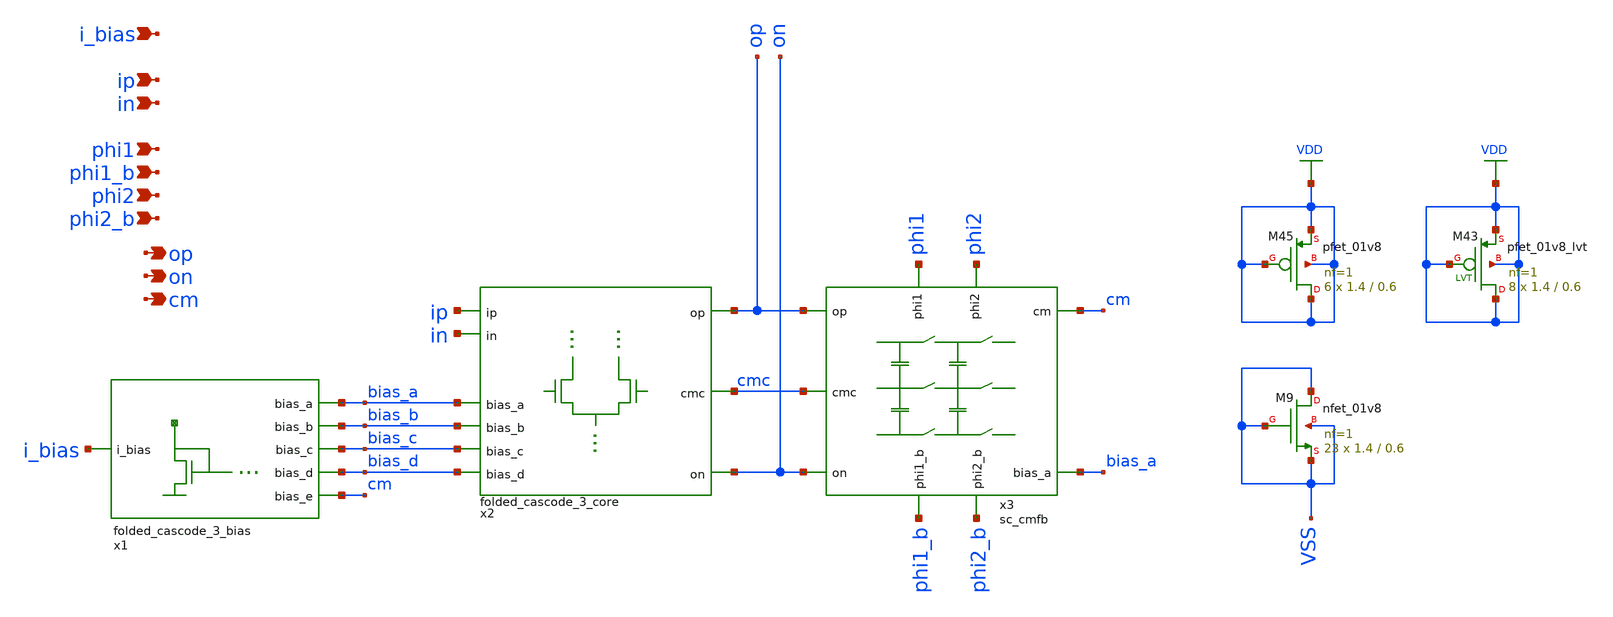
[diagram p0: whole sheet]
** sch_path: design/analog_modulator/schematic/ota.sch
**.subckt ota ip in phi1 phi1_b phi2 phi2_b op on i_bias cm
*.ipin ip
*.ipin in
*.ipin phi1
*.ipin phi1_b
*.ipin phi2
*.ipin phi2_b
*.opin op
*.opin on
*.ipin i_bias
*.opin cm
x1 bias_a bias_b bias_c bias_d cm i_bias VDD VSS folded_cascode_3_bias
x3 phi1 phi1_b op on cm bias_a cmc phi2 phi2_b VDD VSS sc_cmfb
x2 cmc ip in bias_a bias_b bias_c bias_d op on VDD VSS folded_cascode_3_core
XM43 VDD VDD VDD VDD sky130_fd_pr__pfet_01v8_lvt L=0.6 W=1.4 nf=1 ad='int((nf+1)/2) * W/nf * 0.29' as='int((nf+2)/2) * W/nf * 0.29'
+ pd='2*int((nf+1)/2) * (W/nf + 0.29)' ps='2*int((nf+2)/2) * (W/nf + 0.29)' nrd='0.29 / W' nrs='0.29 / W'
+ sa=0 sb=0 sd=0 mult=8 m=8
XM45 VDD VDD VDD VDD sky130_fd_pr__pfet_01v8 L=0.6 W=1.4 nf=1 ad='int((nf+1)/2) * W/nf * 0.29' as='int((nf+2)/2) * W/nf * 0.29'
+ pd='2*int((nf+1)/2) * (W/nf + 0.29)' ps='2*int((nf+2)/2) * (W/nf + 0.29)' nrd='0.29 / W' nrs='0.29 / W'
+ sa=0 sb=0 sd=0 mult=6 m=6
XM9 VSS VSS VSS VSS sky130_fd_pr__nfet_01v8 L=0.6 W=1.4 nf=1 ad='int((nf+1)/2) * W/nf * 0.29' as='int((nf+2)/2) * W/nf * 0.29'
+ pd='2*int((nf+1)/2) * (W/nf + 0.29)' ps='2*int((nf+2)/2) * (W/nf + 0.29)' nrd='0.29 / W' nrs='0.29 / W'
+ sa=0 sb=0 sd=0 mult=23 m=23
**.ends

* expanding   symbol:  folded_cascode_3_bias.sym # of pins=6
** sym_path: design/analog_modulator/schematic/folded_cascode_3_bias.sym
** sch_path: design/analog_modulator/schematic/folded_cascode_3_bias.sch
.subckt folded_cascode_3_bias bias_a bias_b bias_c bias_d bias_e i_bias VDD VSS
*.opin bias_a
*.opin bias_b
*.opin bias_c
*.opin bias_d
*.opin bias_e
*.ipin i_bias
XM22 bias_b bias_c m21d VDD sky130_fd_pr__pfet_01v8 L=0.6 W=1.4 nf=1 ad='int((nf+1)/2) * W/nf * 0.29'
+ as='int((nf+2)/2) * W/nf * 0.29' pd='2*int((nf+1)/2) * (W/nf + 0.29)' ps='2*int((nf+2)/2) * (W/nf + 0.29)'
+ nrd='0.29 / W' nrs='0.29 / W' sa=0 sb=0 sd=0 mult=6 m=6
XM26 m2d bias_c m25d VDD sky130_fd_pr__pfet_01v8 L=0.6 W=1.4 nf=1 ad='int((nf+1)/2) * W/nf * 0.29' as='int((nf+2)/2) * W/nf * 0.29'
+ pd='2*int((nf+1)/2) * (W/nf + 0.29)' ps='2*int((nf+2)/2) * (W/nf + 0.29)' nrd='0.29 / W' nrs='0.29 / W'
+ sa=0 sb=0 sd=0 mult=6 m=6
XM32 bias_e bias_c m31d VDD sky130_fd_pr__pfet_01v8 L=0.6 W=1.4 nf=1 ad='int((nf+1)/2) * W/nf * 0.29'
+ as='int((nf+2)/2) * W/nf * 0.29' pd='2*int((nf+1)/2) * (W/nf + 0.29)' ps='2*int((nf+2)/2) * (W/nf + 0.29)'
+ nrd='0.29 / W' nrs='0.29 / W' sa=0 sb=0 sd=0 mult=6 m=6
XM21 m21d bias_b VDD VDD sky130_fd_pr__pfet_01v8_lvt L=0.6 W=1.4 nf=1 ad='int((nf+1)/2) * W/nf * 0.29'
+ as='int((nf+2)/2) * W/nf * 0.29' pd='2*int((nf+1)/2) * (W/nf + 0.29)' ps='2*int((nf+2)/2) * (W/nf + 0.29)'
+ nrd='0.29 / W' nrs='0.29 / W' sa=0 sb=0 sd=0 mult=6 m=6
XM25 m25d bias_b VDD VDD sky130_fd_pr__pfet_01v8_lvt L=0.6 W=1.4 nf=1 ad='int((nf+1)/2) * W/nf * 0.29'
+ as='int((nf+2)/2) * W/nf * 0.29' pd='2*int((nf+1)/2) * (W/nf + 0.29)' ps='2*int((nf+2)/2) * (W/nf + 0.29)'
+ nrd='0.29 / W' nrs='0.29 / W' sa=0 sb=0 sd=0 mult=6 m=6
XM31 m31d bias_b VDD VDD sky130_fd_pr__pfet_01v8_lvt L=0.6 W=1.4 nf=1 ad='int((nf+1)/2) * W/nf * 0.29'
+ as='int((nf+2)/2) * W/nf * 0.29' pd='2*int((nf+1)/2) * (W/nf + 0.29)' ps='2*int((nf+2)/2) * (W/nf + 0.29)'
+ nrd='0.29 / W' nrs='0.29 / W' sa=0 sb=0 sd=0 mult=6 m=6
XM1 bias_b bias_b bias_c VSS sky130_fd_pr__nfet_01v8_lvt L=0.6 W=1.4 nf=1 ad='int((nf+1)/2) * W/nf * 0.29'
+ as='int((nf+2)/2) * W/nf * 0.29' pd='2*int((nf+1)/2) * (W/nf + 0.29)' ps='2*int((nf+2)/2) * (W/nf + 0.29)'
+ nrd='0.29 / W' nrs='0.29 / W' sa=0 sb=0 sd=0 mult=56 m=56
XM2 m2d m2d bias_d VSS sky130_fd_pr__nfet_01v8 L=0.6 W=1.4 nf=1 ad='int((nf+1)/2) * W/nf * 0.29' as='int((nf+2)/2) * W/nf * 0.29'
+ pd='2*int((nf+1)/2) * (W/nf + 0.29)' ps='2*int((nf+2)/2) * (W/nf + 0.29)' nrd='0.29 / W' nrs='0.29 / W'
+ sa=0 sb=0 sd=0 mult=50 m=50
XM3 bias_d m2d bias_a VSS sky130_fd_pr__nfet_01v8 L=0.6 W=1.4 nf=1 ad='int((nf+1)/2) * W/nf * 0.29' as='int((nf+2)/2) * W/nf * 0.29'
+ pd='2*int((nf+1)/2) * (W/nf + 0.29)' ps='2*int((nf+2)/2) * (W/nf + 0.29)' nrd='0.29 / W' nrs='0.29 / W'
+ sa=0 sb=0 sd=0 mult=2 m=2
XM4 bias_a bias_d m5d VSS sky130_fd_pr__nfet_01v8 L=0.6 W=1.4 nf=1 ad='int((nf+1)/2) * W/nf * 0.29' as='int((nf+2)/2) * W/nf * 0.29'
+ pd='2*int((nf+1)/2) * (W/nf + 0.29)' ps='2*int((nf+2)/2) * (W/nf + 0.29)' nrd='0.29 / W' nrs='0.29 / W'
+ sa=0 sb=0 sd=0 mult=18 m=18
XM5 m5d bias_a VSS VSS sky130_fd_pr__nfet_01v8 L=0.6 W=1.4 nf=1 ad='int((nf+1)/2) * W/nf * 0.29' as='int((nf+2)/2) * W/nf * 0.29'
+ pd='2*int((nf+1)/2) * (W/nf + 0.29)' ps='2*int((nf+2)/2) * (W/nf + 0.29)' nrd='0.29 / W' nrs='0.29 / W'
+ sa=0 sb=0 sd=0 mult=18 m=18
XM6 bias_c i_bias VSS VSS sky130_fd_pr__nfet_01v8 L=0.6 W=1.4 nf=1 ad='int((nf+1)/2) * W/nf * 0.29' as='int((nf+2)/2) * W/nf * 0.29'
+ pd='2*int((nf+1)/2) * (W/nf + 0.29)' ps='2*int((nf+2)/2) * (W/nf + 0.29)' nrd='0.29 / W' nrs='0.29 / W'
+ sa=0 sb=0 sd=0 mult=18 m=18
XM7 i_bias i_bias VSS VSS sky130_fd_pr__nfet_01v8 L=0.6 W=1.4 nf=1 ad='int((nf+1)/2) * W/nf * 0.29' as='int((nf+2)/2) * W/nf * 0.29'
+ pd='2*int((nf+1)/2) * (W/nf + 0.29)' ps='2*int((nf+2)/2) * (W/nf + 0.29)' nrd='0.29 / W' nrs='0.29 / W'
+ sa=0 sb=0 sd=0 mult=18 m=18
XM33 bias_e bias_e net1 VSS sky130_fd_pr__nfet_01v8 L=0.6 W=1.4 nf=1 ad='int((nf+1)/2) * W/nf * 0.29'
+ as='int((nf+2)/2) * W/nf * 0.29' pd='2*int((nf+1)/2) * (W/nf + 0.29)' ps='2*int((nf+2)/2) * (W/nf + 0.29)'
+ nrd='0.29 / W' nrs='0.29 / W' sa=0 sb=0 sd=0 mult=1 m=1
XM49 net1 bias_e net2 VSS sky130_fd_pr__nfet_01v8 L=0.6 W=1.4 nf=1 ad='int((nf+1)/2) * W/nf * 0.29' as='int((nf+2)/2) * W/nf * 0.29'
+ pd='2*int((nf+1)/2) * (W/nf + 0.29)' ps='2*int((nf+2)/2) * (W/nf + 0.29)' nrd='0.29 / W' nrs='0.29 / W'
+ sa=0 sb=0 sd=0 mult=1 m=1
XM50 net2 bias_e net3 VSS sky130_fd_pr__nfet_01v8 L=0.6 W=1.4 nf=1 ad='int((nf+1)/2) * W/nf * 0.29' as='int((nf+2)/2) * W/nf * 0.29'
+ pd='2*int((nf+1)/2) * (W/nf + 0.29)' ps='2*int((nf+2)/2) * (W/nf + 0.29)' nrd='0.29 / W' nrs='0.29 / W'
+ sa=0 sb=0 sd=0 mult=1 m=1
XM63 net3 bias_e VSS VSS sky130_fd_pr__nfet_01v8 L=0.6 W=1.4 nf=1 ad='int((nf+1)/2) * W/nf * 0.29' as='int((nf+2)/2) * W/nf * 0.29'
+ pd='2*int((nf+1)/2) * (W/nf + 0.29)' ps='2*int((nf+2)/2) * (W/nf + 0.29)' nrd='0.29 / W' nrs='0.29 / W'
+ sa=0 sb=0 sd=0 mult=1 m=1
XM68 bias_e bias_e net4 VSS sky130_fd_pr__nfet_01v8 L=0.6 W=1.4 nf=1 ad='int((nf+1)/2) * W/nf * 0.29'
+ as='int((nf+2)/2) * W/nf * 0.29' pd='2*int((nf+1)/2) * (W/nf + 0.29)' ps='2*int((nf+2)/2) * (W/nf + 0.29)'
+ nrd='0.29 / W' nrs='0.29 / W' sa=0 sb=0 sd=0 mult=1 m=1
XM69 net4 bias_e net5 VSS sky130_fd_pr__nfet_01v8 L=0.6 W=1.4 nf=1 ad='int((nf+1)/2) * W/nf * 0.29' as='int((nf+2)/2) * W/nf * 0.29'
+ pd='2*int((nf+1)/2) * (W/nf + 0.29)' ps='2*int((nf+2)/2) * (W/nf + 0.29)' nrd='0.29 / W' nrs='0.29 / W'
+ sa=0 sb=0 sd=0 mult=1 m=1
XM70 net5 bias_e net6 VSS sky130_fd_pr__nfet_01v8 L=0.6 W=1.4 nf=1 ad='int((nf+1)/2) * W/nf * 0.29' as='int((nf+2)/2) * W/nf * 0.29'
+ pd='2*int((nf+1)/2) * (W/nf + 0.29)' ps='2*int((nf+2)/2) * (W/nf + 0.29)' nrd='0.29 / W' nrs='0.29 / W'
+ sa=0 sb=0 sd=0 mult=1 m=1
XM71 net6 bias_e VSS VSS sky130_fd_pr__nfet_01v8 L=0.6 W=1.4 nf=1 ad='int((nf+1)/2) * W/nf * 0.29' as='int((nf+2)/2) * W/nf * 0.29'
+ pd='2*int((nf+1)/2) * (W/nf + 0.29)' ps='2*int((nf+2)/2) * (W/nf + 0.29)' nrd='0.29 / W' nrs='0.29 / W'
+ sa=0 sb=0 sd=0 mult=1 m=1
XM72 bias_e bias_e net7 VSS sky130_fd_pr__nfet_01v8 L=0.6 W=1.4 nf=1 ad='int((nf+1)/2) * W/nf * 0.29'
+ as='int((nf+2)/2) * W/nf * 0.29' pd='2*int((nf+1)/2) * (W/nf + 0.29)' ps='2*int((nf+2)/2) * (W/nf + 0.29)'
+ nrd='0.29 / W' nrs='0.29 / W' sa=0 sb=0 sd=0 mult=1 m=1
XM73 net7 bias_e net8 VSS sky130_fd_pr__nfet_01v8 L=0.6 W=1.4 nf=1 ad='int((nf+1)/2) * W/nf * 0.29' as='int((nf+2)/2) * W/nf * 0.29'
+ pd='2*int((nf+1)/2) * (W/nf + 0.29)' ps='2*int((nf+2)/2) * (W/nf + 0.29)' nrd='0.29 / W' nrs='0.29 / W'
+ sa=0 sb=0 sd=0 mult=1 m=1
XM74 net8 bias_e net9 VSS sky130_fd_pr__nfet_01v8 L=0.6 W=1.4 nf=1 ad='int((nf+1)/2) * W/nf * 0.29' as='int((nf+2)/2) * W/nf * 0.29'
+ pd='2*int((nf+1)/2) * (W/nf + 0.29)' ps='2*int((nf+2)/2) * (W/nf + 0.29)' nrd='0.29 / W' nrs='0.29 / W'
+ sa=0 sb=0 sd=0 mult=1 m=1
XM75 net9 bias_e VSS VSS sky130_fd_pr__nfet_01v8 L=0.6 W=1.4 nf=1 ad='int((nf+1)/2) * W/nf * 0.29' as='int((nf+2)/2) * W/nf * 0.29'
+ pd='2*int((nf+1)/2) * (W/nf + 0.29)' ps='2*int((nf+2)/2) * (W/nf + 0.29)' nrd='0.29 / W' nrs='0.29 / W'
+ sa=0 sb=0 sd=0 mult=1 m=1
XM76 bias_e bias_e net10 VSS sky130_fd_pr__nfet_01v8 L=0.6 W=1.4 nf=1 ad='int((nf+1)/2) * W/nf * 0.29'
+ as='int((nf+2)/2) * W/nf * 0.29' pd='2*int((nf+1)/2) * (W/nf + 0.29)' ps='2*int((nf+2)/2) * (W/nf + 0.29)'
+ nrd='0.29 / W' nrs='0.29 / W' sa=0 sb=0 sd=0 mult=1 m=1
XM77 net10 bias_e net11 VSS sky130_fd_pr__nfet_01v8 L=0.6 W=1.4 nf=1 ad='int((nf+1)/2) * W/nf * 0.29'
+ as='int((nf+2)/2) * W/nf * 0.29' pd='2*int((nf+1)/2) * (W/nf + 0.29)' ps='2*int((nf+2)/2) * (W/nf + 0.29)'
+ nrd='0.29 / W' nrs='0.29 / W' sa=0 sb=0 sd=0 mult=1 m=1
XM78 net11 bias_e net12 VSS sky130_fd_pr__nfet_01v8 L=0.6 W=1.4 nf=1 ad='int((nf+1)/2) * W/nf * 0.29'
+ as='int((nf+2)/2) * W/nf * 0.29' pd='2*int((nf+1)/2) * (W/nf + 0.29)' ps='2*int((nf+2)/2) * (W/nf + 0.29)'
+ nrd='0.29 / W' nrs='0.29 / W' sa=0 sb=0 sd=0 mult=1 m=1
XM79 net12 bias_e VSS VSS sky130_fd_pr__nfet_01v8 L=0.6 W=1.4 nf=1 ad='int((nf+1)/2) * W/nf * 0.29' as='int((nf+2)/2) * W/nf * 0.29'
+ pd='2*int((nf+1)/2) * (W/nf + 0.29)' ps='2*int((nf+2)/2) * (W/nf + 0.29)' nrd='0.29 / W' nrs='0.29 / W'
+ sa=0 sb=0 sd=0 mult=1 m=1
XM64 bias_e bias_e net13 VSS sky130_fd_pr__nfet_01v8 L=0.6 W=1.4 nf=1 ad='int((nf+1)/2) * W/nf * 0.29'
+ as='int((nf+2)/2) * W/nf * 0.29' pd='2*int((nf+1)/2) * (W/nf + 0.29)' ps='2*int((nf+2)/2) * (W/nf + 0.29)'
+ nrd='0.29 / W' nrs='0.29 / W' sa=0 sb=0 sd=0 mult=1 m=1
XM65 net13 bias_e net14 VSS sky130_fd_pr__nfet_01v8 L=0.6 W=1.4 nf=1 ad='int((nf+1)/2) * W/nf * 0.29'
+ as='int((nf+2)/2) * W/nf * 0.29' pd='2*int((nf+1)/2) * (W/nf + 0.29)' ps='2*int((nf+2)/2) * (W/nf + 0.29)'
+ nrd='0.29 / W' nrs='0.29 / W' sa=0 sb=0 sd=0 mult=1 m=1
XM66 net14 bias_e net15 VSS sky130_fd_pr__nfet_01v8 L=0.6 W=1.4 nf=1 ad='int((nf+1)/2) * W/nf * 0.29'
+ as='int((nf+2)/2) * W/nf * 0.29' pd='2*int((nf+1)/2) * (W/nf + 0.29)' ps='2*int((nf+2)/2) * (W/nf + 0.29)'
+ nrd='0.29 / W' nrs='0.29 / W' sa=0 sb=0 sd=0 mult=1 m=1
XM67 net15 bias_e VSS VSS sky130_fd_pr__nfet_01v8 L=0.6 W=1.4 nf=1 ad='int((nf+1)/2) * W/nf * 0.29' as='int((nf+2)/2) * W/nf * 0.29'
+ pd='2*int((nf+1)/2) * (W/nf + 0.29)' ps='2*int((nf+2)/2) * (W/nf + 0.29)' nrd='0.29 / W' nrs='0.29 / W'
+ sa=0 sb=0 sd=0 mult=1 m=1
XM57 bias_b VDD VDD VDD sky130_fd_pr__pfet_01v8 L=0.6 W=1.4 nf=1 ad='int((nf+1)/2) * W/nf * 0.29' as='int((nf+2)/2) * W/nf * 0.29'
+ pd='2*int((nf+1)/2) * (W/nf + 0.29)' ps='2*int((nf+2)/2) * (W/nf + 0.29)' nrd='0.29 / W' nrs='0.29 / W'
+ sa=0 sb=0 sd=0 mult=2 m=2
XM58 m2d VDD VDD VDD sky130_fd_pr__pfet_01v8 L=0.6 W=1.4 nf=1 ad='int((nf+1)/2) * W/nf * 0.29' as='int((nf+2)/2) * W/nf * 0.29'
+ pd='2*int((nf+1)/2) * (W/nf + 0.29)' ps='2*int((nf+2)/2) * (W/nf + 0.29)' nrd='0.29 / W' nrs='0.29 / W'
+ sa=0 sb=0 sd=0 mult=2 m=2
XM59 bias_e VDD VDD VDD sky130_fd_pr__pfet_01v8 L=0.6 W=1.4 nf=1 ad='int((nf+1)/2) * W/nf * 0.29' as='int((nf+2)/2) * W/nf * 0.29'
+ pd='2*int((nf+1)/2) * (W/nf + 0.29)' ps='2*int((nf+2)/2) * (W/nf + 0.29)' nrd='0.29 / W' nrs='0.29 / W'
+ sa=0 sb=0 sd=0 mult=2 m=2
XM60 m31d VDD VDD VDD sky130_fd_pr__pfet_01v8 L=0.6 W=1.4 nf=1 ad='int((nf+1)/2) * W/nf * 0.29' as='int((nf+2)/2) * W/nf * 0.29'
+ pd='2*int((nf+1)/2) * (W/nf + 0.29)' ps='2*int((nf+2)/2) * (W/nf + 0.29)' nrd='0.29 / W' nrs='0.29 / W'
+ sa=0 sb=0 sd=0 mult=2 m=2
XM42 m5d VSS VSS VSS sky130_fd_pr__nfet_01v8 L=0.6 W=1.4 nf=1 ad='int((nf+1)/2) * W/nf * 0.29' as='int((nf+2)/2) * W/nf * 0.29'
+ pd='2*int((nf+1)/2) * (W/nf + 0.29)' ps='2*int((nf+2)/2) * (W/nf + 0.29)' nrd='0.29 / W' nrs='0.29 / W'
+ sa=0 sb=0 sd=0 mult=6 m=6
XM44 bias_c bias_c bias_c VSS sky130_fd_pr__nfet_01v8 L=0.6 W=1.4 nf=1 ad='int((nf+1)/2) * W/nf * 0.29'
+ as='int((nf+2)/2) * W/nf * 0.29' pd='2*int((nf+1)/2) * (W/nf + 0.29)' ps='2*int((nf+2)/2) * (W/nf + 0.29)'
+ nrd='0.29 / W' nrs='0.29 / W' sa=0 sb=0 sd=0 mult=2 m=2
XM34 bias_d bias_d bias_d VSS sky130_fd_pr__nfet_01v8 L=0.6 W=1.4 nf=1 ad='int((nf+1)/2) * W/nf * 0.29'
+ as='int((nf+2)/2) * W/nf * 0.29' pd='2*int((nf+1)/2) * (W/nf + 0.29)' ps='2*int((nf+2)/2) * (W/nf + 0.29)'
+ nrd='0.29 / W' nrs='0.29 / W' sa=0 sb=0 sd=0 mult=8 m=8
XM35 m2d m2d m2d VSS sky130_fd_pr__nfet_01v8 L=0.6 W=1.4 nf=1 ad='int((nf+1)/2) * W/nf * 0.29' as='int((nf+2)/2) * W/nf * 0.29'
+ pd='2*int((nf+1)/2) * (W/nf + 0.29)' ps='2*int((nf+2)/2) * (W/nf + 0.29)' nrd='0.29 / W' nrs='0.29 / W'
+ sa=0 sb=0 sd=0 mult=2 m=2
XM36 bias_a bias_a bias_a VSS sky130_fd_pr__nfet_01v8 L=0.6 W=1.4 nf=1 ad='int((nf+1)/2) * W/nf * 0.29'
+ as='int((nf+2)/2) * W/nf * 0.29' pd='2*int((nf+1)/2) * (W/nf + 0.29)' ps='2*int((nf+2)/2) * (W/nf + 0.29)'
+ nrd='0.29 / W' nrs='0.29 / W' sa=0 sb=0 sd=0 mult=4 m=4
XM37 bias_e bias_e bias_e VSS sky130_fd_pr__nfet_01v8 L=0.6 W=1.4 nf=1 ad='int((nf+1)/2) * W/nf * 0.29'
+ as='int((nf+2)/2) * W/nf * 0.29' pd='2*int((nf+1)/2) * (W/nf + 0.29)' ps='2*int((nf+2)/2) * (W/nf + 0.29)'
+ nrd='0.29 / W' nrs='0.29 / W' sa=0 sb=0 sd=0 mult=8 m=8
XM54 m25d m25d m25d VDD sky130_fd_pr__pfet_01v8 L=0.6 W=1.4 nf=1 ad='int((nf+1)/2) * W/nf * 0.29' as='int((nf+2)/2) * W/nf * 0.29'
+ pd='2*int((nf+1)/2) * (W/nf + 0.29)' ps='2*int((nf+2)/2) * (W/nf + 0.29)' nrd='0.29 / W' nrs='0.29 / W'
+ sa=0 sb=0 sd=0 mult=2 m=2
XM29 m5d m5d m5d VSS sky130_fd_pr__nfet_01v8 L=0.6 W=1.4 nf=1 ad='int((nf+1)/2) * W/nf * 0.29' as='int((nf+2)/2) * W/nf * 0.29'
+ pd='2*int((nf+1)/2) * (W/nf + 0.29)' ps='2*int((nf+2)/2) * (W/nf + 0.29)' nrd='0.29 / W' nrs='0.29 / W'
+ sa=0 sb=0 sd=0 mult=6 m=6
XM8 i_bias i_bias i_bias VSS sky130_fd_pr__nfet_01v8 L=0.6 W=1.4 nf=1 ad='int((nf+1)/2) * W/nf * 0.29'
+ as='int((nf+2)/2) * W/nf * 0.29' pd='2*int((nf+1)/2) * (W/nf + 0.29)' ps='2*int((nf+2)/2) * (W/nf + 0.29)'
+ nrd='0.29 / W' nrs='0.29 / W' sa=0 sb=0 sd=0 mult=2 m=2
XM10 bias_c bias_c bias_c VSS sky130_fd_pr__nfet_01v8_lvt L=0.6 W=1.4 nf=1 ad='int((nf+1)/2) * W/nf * 0.29'
+ as='int((nf+2)/2) * W/nf * 0.29' pd='2*int((nf+1)/2) * (W/nf + 0.29)' ps='2*int((nf+2)/2) * (W/nf + 0.29)'
+ nrd='0.29 / W' nrs='0.29 / W' sa=0 sb=0 sd=0 mult=8 m=8
XM27 bias_b bias_b bias_b VSS sky130_fd_pr__nfet_01v8_lvt L=0.6 W=1.4 nf=1 ad='int((nf+1)/2) * W/nf * 0.29'
+ as='int((nf+2)/2) * W/nf * 0.29' pd='2*int((nf+1)/2) * (W/nf + 0.29)' ps='2*int((nf+2)/2) * (W/nf + 0.29)'
+ nrd='0.29 / W' nrs='0.29 / W' sa=0 sb=0 sd=0 mult=8 m=8
XM46 m21d m21d m21d VDD sky130_fd_pr__pfet_01v8_lvt L=0.6 W=1.4 nf=1 ad='int((nf+1)/2) * W/nf * 0.29'
+ as='int((nf+2)/2) * W/nf * 0.29' pd='2*int((nf+1)/2) * (W/nf + 0.29)' ps='2*int((nf+2)/2) * (W/nf + 0.29)'
+ nrd='0.29 / W' nrs='0.29 / W' sa=0 sb=0 sd=0 mult=2 m=2
XM47 m25d m25d m25d VDD sky130_fd_pr__pfet_01v8_lvt L=0.6 W=1.4 nf=1 ad='int((nf+1)/2) * W/nf * 0.29'
+ as='int((nf+2)/2) * W/nf * 0.29' pd='2*int((nf+1)/2) * (W/nf + 0.29)' ps='2*int((nf+2)/2) * (W/nf + 0.29)'
+ nrd='0.29 / W' nrs='0.29 / W' sa=0 sb=0 sd=0 mult=2 m=2
XM48 m31d m31d m31d VDD sky130_fd_pr__pfet_01v8_lvt L=0.6 W=1.4 nf=1 ad='int((nf+1)/2) * W/nf * 0.29'
+ as='int((nf+2)/2) * W/nf * 0.29' pd='2*int((nf+1)/2) * (W/nf + 0.29)' ps='2*int((nf+2)/2) * (W/nf + 0.29)'
+ nrd='0.29 / W' nrs='0.29 / W' sa=0 sb=0 sd=0 mult=2 m=2
XM51 m21d m21d m21d VDD sky130_fd_pr__pfet_01v8 L=0.6 W=1.4 nf=1 ad='int((nf+1)/2) * W/nf * 0.29' as='int((nf+2)/2) * W/nf * 0.29'
+ pd='2*int((nf+1)/2) * (W/nf + 0.29)' ps='2*int((nf+2)/2) * (W/nf + 0.29)' nrd='0.29 / W' nrs='0.29 / W'
+ sa=0 sb=0 sd=0 mult=2 m=2
.ends


* expanding   symbol:  sc_cmfb.sym # of pins=9
** sym_path: design/analog_modulator/schematic/sc_cmfb.sym
** sch_path: design/analog_modulator/schematic/sc_cmfb.sch
.subckt sc_cmfb phi1 phi1_b op on cm bias_a cmc phi2 phi2_b VDD VSS
*.ipin on
*.ipin cm
*.ipin bias_a
*.ipin op
*.opin cmc
*.ipin phi2_b
*.ipin phi2
*.ipin phi1_b
*.ipin phi1
XC3 op cmc sky130_fd_pr__cap_mim_m3_1 W=4.8 L=4.8 MF=4 m=4
XC4 on cmc sky130_fd_pr__cap_mim_m3_1 W=4.8 L=4.8 MF=4 m=4
x1 net1 op phi2 phi2_b VDD VSS 1 5.3 0.15 13.7 0.15 transmission_gate
x2 net2 cmc phi2 phi2_b VDD VSS 1 5.3 0.15 13.7 0.15 transmission_gate
x3 net3 on phi2 phi2_b VDD VSS 1 5.3 0.15 13.7 0.15 transmission_gate
x4 cm net1 phi1 phi1_b VDD VSS 1 5.3 0.15 13.7 0.15 transmission_gate
x5 bias_a net2 phi1 phi1_b VDD VSS 1 5.3 0.15 13.7 0.15 transmission_gate
x6 cm net3 phi1 phi1_b VDD VSS 1 5.3 0.15 13.7 0.15 transmission_gate
XC1 net1 net2 sky130_fd_pr__cap_mim_m3_1 W=4.8 L=4.8 MF=2 m=2
XC2 net3 net2 sky130_fd_pr__cap_mim_m3_1 W=4.8 L=4.8 MF=2 m=2
x7 cm net4 phi2 phi2_b VDD VSS 1 5.3 0.15 13.7 0.15 transmission_gate
x8 bias_a net5 phi2 phi2_b VDD VSS 1 5.3 0.15 13.7 0.15 transmission_gate
x9 cm net6 phi2 phi2_b VDD VSS 1 5.3 0.15 13.7 0.15 transmission_gate
x10 net4 op phi1 phi1_b VDD VSS 1 5.3 0.15 13.7 0.15 transmission_gate
x11 net5 cmc phi1 phi1_b VDD VSS 1 5.3 0.15 13.7 0.15 transmission_gate
x12 net6 on phi1 phi1_b VDD VSS 1 5.3 0.15 13.7 0.15 transmission_gate
XC5 net4 net5 sky130_fd_pr__cap_mim_m3_1 W=4.8 L=4.8 MF=2 m=2
XC6 net6 net5 sky130_fd_pr__cap_mim_m3_1 W=4.8 L=4.8 MF=2 m=2
XCdummy net7 net8 sky130_fd_pr__cap_mim_m3_1 W=4.8 L=4.8 MF=20 m=20
.ends


* expanding   symbol:  folded_cascode_3_core.sym # of pins=9
** sym_path: design/schematic/folded_cascode_3_core.sym
** sch_path: design/schematic/folded_cascode_3_core.sch
.subckt folded_cascode_3_core cmc ip in bias_a bias_b bias_c bias_d op on VDD VSS
*.ipin cmc
*.ipin ip
*.ipin in
*.ipin bias_a
*.ipin bias_b
*.ipin bias_c
*.ipin bias_d
*.opin op
*.opin on
XM1 net2 ip net1 VSS sky130_fd_pr__nfet_01v8_lvt L=0.2 W=1.2 nf=1 ad='int((nf+1)/2) * W/nf * 0.29' as='int((nf+2)/2) * W/nf * 0.29'
+ pd='2*int((nf+1)/2) * (W/nf + 0.29)' ps='2*int((nf+2)/2) * (W/nf + 0.29)' nrd='0.29 / W' nrs='0.29 / W'
+ sa=0 sb=0 sd=0 mult=6 m=6
XM2 net3 in net1 VSS sky130_fd_pr__nfet_01v8_lvt L=0.2 W=1.2 nf=1 ad='int((nf+1)/2) * W/nf * 0.29' as='int((nf+2)/2) * W/nf * 0.29'
+ pd='2*int((nf+1)/2) * (W/nf + 0.29)' ps='2*int((nf+2)/2) * (W/nf + 0.29)' nrd='0.29 / W' nrs='0.29 / W'
+ sa=0 sb=0 sd=0 mult=6 m=6
XM6 net1 cmc VSS VSS sky130_fd_pr__nfet_01v8 L=0.6 W=1.4 nf=1 ad='int((nf+1)/2) * W/nf * 0.29' as='int((nf+2)/2) * W/nf * 0.29'
+ pd='2*int((nf+1)/2) * (W/nf + 0.29)' ps='2*int((nf+2)/2) * (W/nf + 0.29)' nrd='0.29 / W' nrs='0.29 / W'
+ sa=0 sb=0 sd=0 mult=96 m=96
XM5 net1 bias_a VSS VSS sky130_fd_pr__nfet_01v8 L=0.6 W=1.4 nf=1 ad='int((nf+1)/2) * W/nf * 0.29' as='int((nf+2)/2) * W/nf * 0.29'
+ pd='2*int((nf+1)/2) * (W/nf + 0.29)' ps='2*int((nf+2)/2) * (W/nf + 0.29)' nrd='0.29 / W' nrs='0.29 / W'
+ sa=0 sb=0 sd=0 mult=96 m=96
XM11 net2 bias_b VDD VDD sky130_fd_pr__pfet_01v8_lvt L=0.6 W=1.4 nf=1 ad='int((nf+1)/2) * W/nf * 0.29'
+ as='int((nf+2)/2) * W/nf * 0.29' pd='2*int((nf+1)/2) * (W/nf + 0.29)' ps='2*int((nf+2)/2) * (W/nf + 0.29)'
+ nrd='0.29 / W' nrs='0.29 / W' sa=0 sb=0 sd=0 mult=24 m=24
XM12 net3 bias_b VDD VDD sky130_fd_pr__pfet_01v8_lvt L=0.6 W=1.4 nf=1 ad='int((nf+1)/2) * W/nf * 0.29'
+ as='int((nf+2)/2) * W/nf * 0.29' pd='2*int((nf+1)/2) * (W/nf + 0.29)' ps='2*int((nf+2)/2) * (W/nf + 0.29)'
+ nrd='0.29 / W' nrs='0.29 / W' sa=0 sb=0 sd=0 mult=24 m=24
XM1A on bias_c net2 VDD sky130_fd_pr__pfet_01v8 L=0.6 W=1.4 nf=1 ad='int((nf+1)/2) * W/nf * 0.29' as='int((nf+2)/2) * W/nf * 0.29'
+ pd='2*int((nf+1)/2) * (W/nf + 0.29)' ps='2*int((nf+2)/2) * (W/nf + 0.29)' nrd='0.29 / W' nrs='0.29 / W'
+ sa=0 sb=0 sd=0 mult=20 m=20
XM8 op bias_c net3 VDD sky130_fd_pr__pfet_01v8 L=0.6 W=1.4 nf=1 ad='int((nf+1)/2) * W/nf * 0.29' as='int((nf+2)/2) * W/nf * 0.29'
+ pd='2*int((nf+1)/2) * (W/nf + 0.29)' ps='2*int((nf+2)/2) * (W/nf + 0.29)' nrd='0.29 / W' nrs='0.29 / W'
+ sa=0 sb=0 sd=0 mult=20 m=20
XM3A on bias_d net4 VSS sky130_fd_pr__nfet_01v8 L=0.6 W=1.4 nf=1 ad='int((nf+1)/2) * W/nf * 0.29' as='int((nf+2)/2) * W/nf * 0.29'
+ pd='2*int((nf+1)/2) * (W/nf + 0.29)' ps='2*int((nf+2)/2) * (W/nf + 0.29)' nrd='0.29 / W' nrs='0.29 / W'
+ sa=0 sb=0 sd=0 mult=36 m=36
XM7 op bias_d net5 VSS sky130_fd_pr__nfet_01v8 L=0.6 W=1.4 nf=1 ad='int((nf+1)/2) * W/nf * 0.29' as='int((nf+2)/2) * W/nf * 0.29'
+ pd='2*int((nf+1)/2) * (W/nf + 0.29)' ps='2*int((nf+2)/2) * (W/nf + 0.29)' nrd='0.29 / W' nrs='0.29 / W'
+ sa=0 sb=0 sd=0 mult=36 m=36
XM3 net4 bias_a VSS VSS sky130_fd_pr__nfet_01v8 L=0.6 W=1.4 nf=1 ad='int((nf+1)/2) * W/nf * 0.29' as='int((nf+2)/2) * W/nf * 0.29'
+ pd='2*int((nf+1)/2) * (W/nf + 0.29)' ps='2*int((nf+2)/2) * (W/nf + 0.29)' nrd='0.29 / W' nrs='0.29 / W'
+ sa=0 sb=0 sd=0 mult=36 m=36
XM4 net5 bias_a VSS VSS sky130_fd_pr__nfet_01v8 L=0.6 W=1.4 nf=1 ad='int((nf+1)/2) * W/nf * 0.29' as='int((nf+2)/2) * W/nf * 0.29'
+ pd='2*int((nf+1)/2) * (W/nf + 0.29)' ps='2*int((nf+2)/2) * (W/nf + 0.29)' nrd='0.29 / W' nrs='0.29 / W'
+ sa=0 sb=0 sd=0 mult=36 m=36
.ends


* expanding   symbol:  transmission_gate.sym # of pins=4
** sym_path: design/analog_modulator/schematic/transmission_gate.sym
** sch_path: design/analog_modulator/schematic/transmission_gate.sch
.subckt transmission_gate in out en en_b VDD VSS N W_N L_N W_P L_P    N=1 W_N=5.3 L_N=0.15 W_P=13.7
+ L_P=0.15
*.iopin in
*.iopin out
*.ipin en
*.ipin en_b
XM1 out en in VSS sky130_fd_pr__nfet_01v8 L='L_N' W='W_N' nf=1 ad='int((nf+1)/2) * W/nf * 0.29' as='int((nf+2)/2) * W/nf * 0.29'
+ pd='2*int((nf+1)/2) * (W/nf + 0.29)' ps='2*int((nf+2)/2) * (W/nf + 0.29)' nrd='0.29 / W' nrs='0.29 / W'
+ sa=0 sb=0 sd=0 mult='N' m='N'
XM2 out en_b in VDD sky130_fd_pr__pfet_01v8 L='L_P' W='W_P' nf=1 ad='int((nf+1)/2) * W/nf * 0.29' as='int((nf+2)/2) * W/nf * 0.29'
+ pd='2*int((nf+1)/2) * (W/nf + 0.29)' ps='2*int((nf+2)/2) * (W/nf + 0.29)' nrd='0.29 / W' nrs='0.29 / W'
+ sa=0 sb=0 sd=0 mult='N' m='N'
.ends

.GLOBAL VDD
.end
